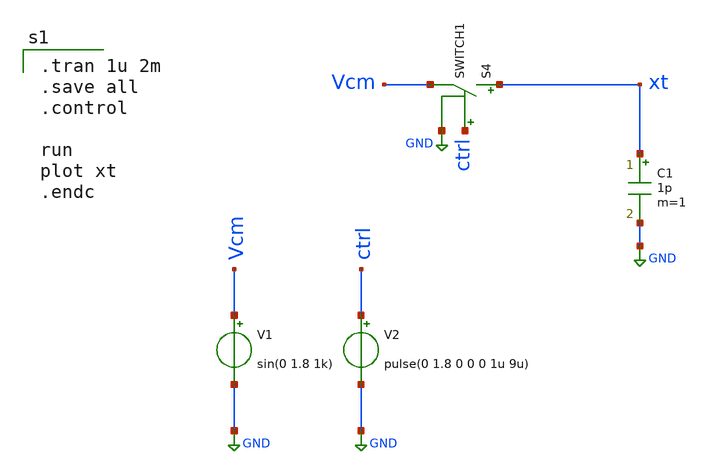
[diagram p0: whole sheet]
** sch_path: Behavioral_model/fftcheck.sch
.lib $::SKYWATER_MODELS/sky130.lib.spice tt
.include $::SKYWATER_STDCELLS/sky130_fd_sc_hd.spice
.model switch1 sw vt=0.5 vh=0 ron=0.1 roff=10000G

**.subckt fftcheck
V1 Vcm GND sin(0 1.8 1k)
S4 xt Vcm ctrl GND SWITCH1
V2 ctrl GND pulse(0 1.8 0 0 0 1u 9u)
C1 xt GND 1p m=1
**** begin user architecture code

.tran 1u 2m
.save all
.control

run
plot xt
.endc

**** end user architecture code
**.ends
.GLOBAL GND
.end
